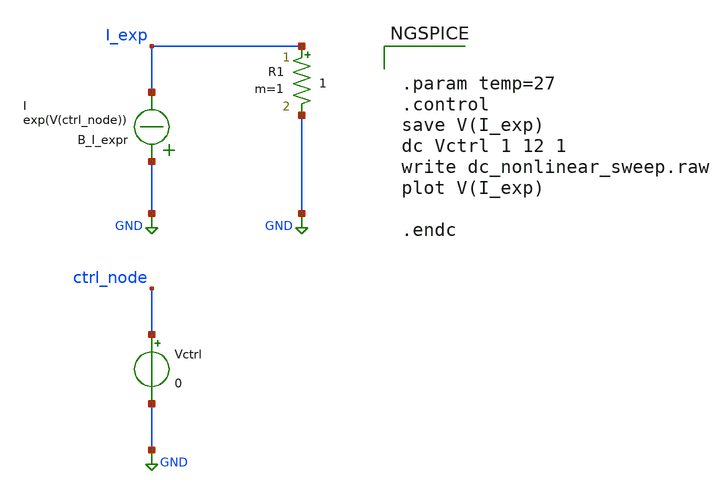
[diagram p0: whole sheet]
** sch_path: test_bench_temp/nonlinear_sweep_dc_tb.sch
**.subckt nonlinear_sweep_dc_tb
B_I_expr GND I_exp I = exp(V(ctrl_node))
Vctrl ctrl_node GND 0
R1 I_exp GND 1 m=1
**** begin user architecture code


.param temp=27
.control
save V(I_exp)
dc Vctrl 1 12 1
write dc_nonlinear_sweep.raw
plot V(I_exp)

.endc


**** end user architecture code
**.ends
.GLOBAL GND
.end
